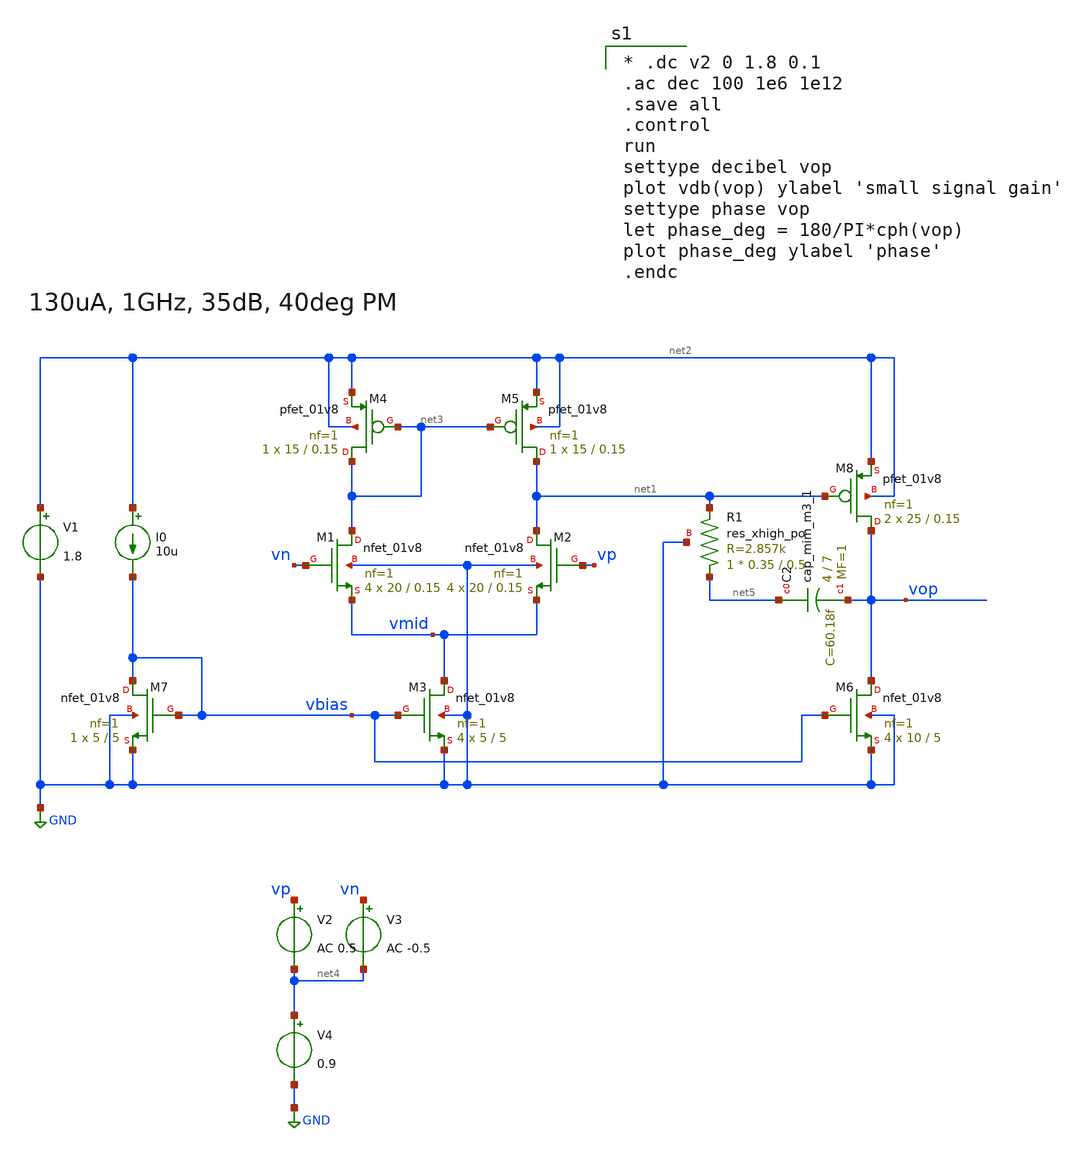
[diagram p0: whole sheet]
** sch_path: xschem/2stage_test.sch
**.subckt 2stage_test
XM1 net3 vn vmid GND sky130_fd_pr__nfet_01v8 L=0.15 W=20 nf=1 ad='int((nf+1)/2) * W/nf * 0.29' as='int((nf+2)/2) * W/nf * 0.29'
+ pd='2*int((nf+1)/2) * (W/nf + 0.29)' ps='2*int((nf+2)/2) * (W/nf + 0.29)' nrd='0.29 / W' nrs='0.29 / W'
+ sa=0 sb=0 sd=0 mult=4 m=4
XM2 net1 vp vmid GND sky130_fd_pr__nfet_01v8 L=0.15 W=20 nf=1 ad='int((nf+1)/2) * W/nf * 0.29' as='int((nf+2)/2) * W/nf * 0.29'
+ pd='2*int((nf+1)/2) * (W/nf + 0.29)' ps='2*int((nf+2)/2) * (W/nf + 0.29)' nrd='0.29 / W' nrs='0.29 / W'
+ sa=0 sb=0 sd=0 mult=4 m=4
XM3 vmid vbias GND GND sky130_fd_pr__nfet_01v8 L=5 W=5 nf=1 ad='int((nf+1)/2) * W/nf * 0.29' as='int((nf+2)/2) * W/nf * 0.29'
+ pd='2*int((nf+1)/2) * (W/nf + 0.29)' ps='2*int((nf+2)/2) * (W/nf + 0.29)' nrd='0.29 / W' nrs='0.29 / W'
+ sa=0 sb=0 sd=0 mult=4 m=4
XM4 net3 net3 net2 net2 sky130_fd_pr__pfet_01v8 L=0.15 W=15 nf=1 ad='int((nf+1)/2) * W/nf * 0.29' as='int((nf+2)/2) * W/nf * 0.29'
+ pd='2*int((nf+1)/2) * (W/nf + 0.29)' ps='2*int((nf+2)/2) * (W/nf + 0.29)' nrd='0.29 / W' nrs='0.29 / W'
+ sa=0 sb=0 sd=0 mult=1 m=1
XM5 net1 net3 net2 net2 sky130_fd_pr__pfet_01v8 L=0.15 W=15 nf=1 ad='int((nf+1)/2) * W/nf * 0.29' as='int((nf+2)/2) * W/nf * 0.29'
+ pd='2*int((nf+1)/2) * (W/nf + 0.29)' ps='2*int((nf+2)/2) * (W/nf + 0.29)' nrd='0.29 / W' nrs='0.29 / W'
+ sa=0 sb=0 sd=0 mult=1 m=1
I0 net2 vbias 10u
XM7 vbias vbias GND GND sky130_fd_pr__nfet_01v8 L=5 W=5 nf=1 ad='int((nf+1)/2) * W/nf * 0.29' as='int((nf+2)/2) * W/nf * 0.29'
+ pd='2*int((nf+1)/2) * (W/nf + 0.29)' ps='2*int((nf+2)/2) * (W/nf + 0.29)' nrd='0.29 / W' nrs='0.29 / W'
+ sa=0 sb=0 sd=0 mult=1 m=1
V2 vp net4 AC 0.5
V3 vn net4 AC -0.5
V4 net4 GND 0.9
V1 net2 GND 1.8
XM6 vop vbias GND GND sky130_fd_pr__nfet_01v8 L=5 W=10 nf=1 ad='int((nf+1)/2) * W/nf * 0.29' as='int((nf+2)/2) * W/nf * 0.29'
+ pd='2*int((nf+1)/2) * (W/nf + 0.29)' ps='2*int((nf+2)/2) * (W/nf + 0.29)' nrd='0.29 / W' nrs='0.29 / W'
+ sa=0 sb=0 sd=0 mult=4 m=4
XM8 vop net1 net2 net2 sky130_fd_pr__pfet_01v8 L=0.15 W=25 nf=1 ad='int((nf+1)/2) * W/nf * 0.29' as='int((nf+2)/2) * W/nf * 0.29'
+ pd='2*int((nf+1)/2) * (W/nf + 0.29)' ps='2*int((nf+2)/2) * (W/nf + 0.29)' nrd='0.29 / W' nrs='0.29 / W'
+ sa=0 sb=0 sd=0 mult=2 m=2
XR1 net5 net1 GND sky130_fd_pr__res_xhigh_po W=0.35 L=0.5 mult=1 m=1
XC2 net5 vop sky130_fd_pr__cap_mim_m3_1 W=4 L=7 MF=1 m=1
**** begin user architecture code
.lib $::SKYWATER_MODELS/sky130.lib.spice tt
.include $::PDKPATH/libs.ref/sky130_fd_sc_hs/spice/sky130_fd_sc_hs.spice


* .dc v2 0 1.8 0.1
.ac dec 100 1e6 1e12
.save all
.control
run
settype decibel vop
plot vdb(vop) ylabel 'small signal gain'
settype phase vop
let phase_deg = 180/PI*cph(vop)
plot phase_deg ylabel 'phase'
.endc


**** end user architecture code
**.ends
.GLOBAL GND
.end
